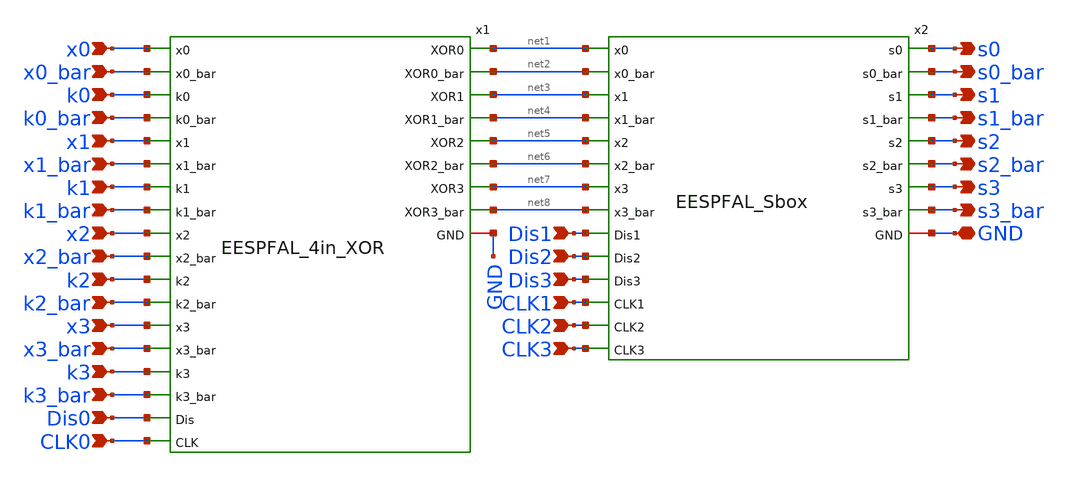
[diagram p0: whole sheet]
** sch_path: skywater_stuff/EESPFAL_PRESENT80_R1.sch
**.subckt EESPFAL_PRESENT80_R1 GND x0 x0_bar k0 k0_bar x1 x1_bar k1 k1_bar x2 x2_bar k2 k2_bar x3
*+ x3_bar k3 k3_bar s0 s0_bar CLK0 Dis0 CLK1 Dis1 s2 s2_bar s3_bar s3 s1_bar s1 CLK3 Dis2 CLK2 Dis3
*.iopin GND
*.ipin x0
*.ipin x0_bar
*.ipin k0
*.ipin k0_bar
*.ipin x1
*.ipin x1_bar
*.ipin k1
*.ipin k1_bar
*.ipin x2
*.ipin x2_bar
*.ipin k2
*.ipin k2_bar
*.ipin x3
*.ipin x3_bar
*.ipin k3
*.ipin k3_bar
*.opin s0
*.opin s0_bar
*.ipin CLK0
*.ipin Dis0
*.ipin CLK1
*.ipin Dis1
*.opin s2
*.opin s2_bar
*.opin s3_bar
*.opin s3
*.opin s1_bar
*.opin s1
*.ipin CLK3
*.ipin Dis2
*.ipin CLK2
*.ipin Dis3
x1 x0 x0_bar k0 k0_bar x1 x1_bar k1 k1_bar x2 x2_bar k2 k2_bar x3 x3_bar k3 k3_bar net2 net1 net4
+ net3 net6 net5 net8 net7 GND CLK0 Dis0 EESPFAL_4in_XOR
x2 GND net1 net2 net3 net4 net5 net6 net7 net8 Dis1 CLK1 CLK2 Dis2 CLK3 Dis3 s0 s0_bar s1_bar s1 s2
+ s2_bar s3_bar s3 EESPFAL_Sbox
**.ends
.end
